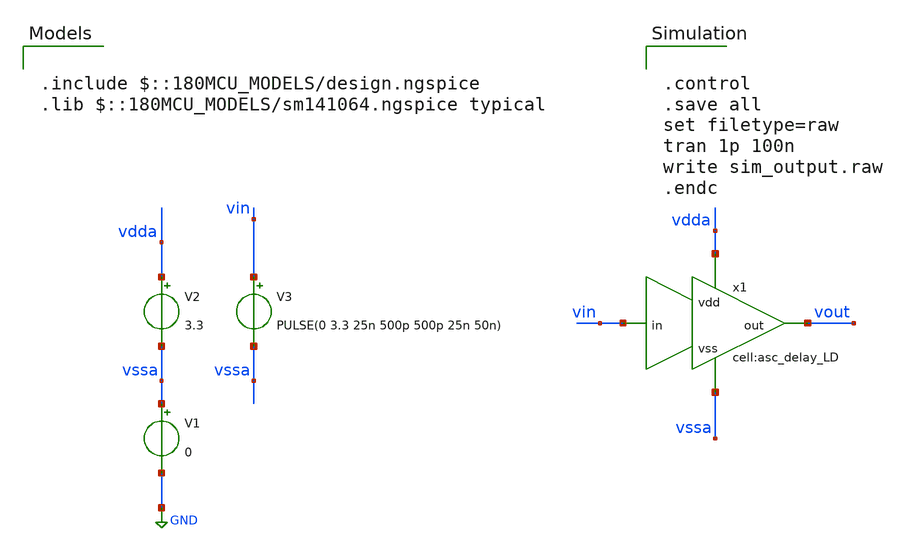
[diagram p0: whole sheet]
** sch_path: designs/libs/tb_analog/tb_asc_delay_1ns/tb_asc_delay_1ns.sch
**.subckt tb_asc_delay_1ns
V1 vssa GND 0
V2 vdda vssa 3.3
V3 vin vssa PULSE(0 3.3 25n 500p 500p 25n 50n)
x1 vin vssa vout vdda asc_delay_LD
**** begin user architecture code

.include $::180MCU_MODELS/design.ngspice
.lib $::180MCU_MODELS/sm141064.ngspice typical



.control
.save all
set filetype=raw
tran 1p 100n
write sim_output.raw
.endc


**** end user architecture code
**.ends
.GLOBAL GND
.end
